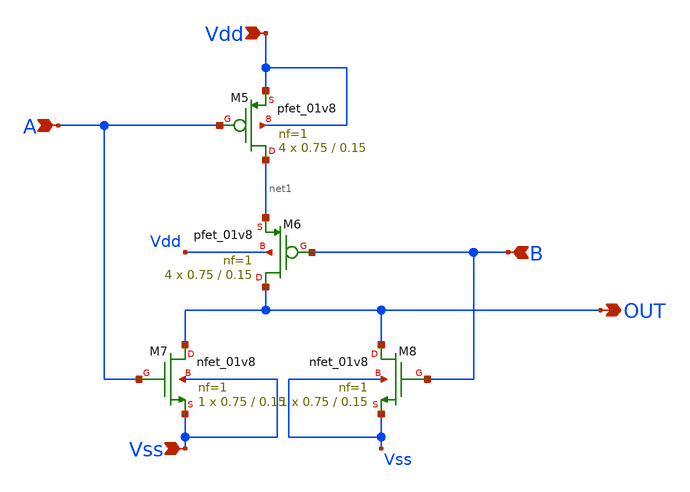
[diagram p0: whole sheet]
** sch_path: icdesign/sch/NOR/NOR.sch
**.subckt NOR Vdd Vss A B OUT
*.ipin Vdd
*.ipin Vss
*.ipin A
*.ipin B
*.opin OUT
XM5 net1 A Vdd Vdd sky130_fd_pr__pfet_01v8 L=0.15 W=0.75 nf=1 ad='int((nf+1)/2) * W/nf * 0.29' as='int((nf+2)/2) * W/nf * 0.29'
+ pd='2*int((nf+1)/2) * (W/nf + 0.29)' ps='2*int((nf+2)/2) * (W/nf + 0.29)' nrd='0.29 / W' nrs='0.29 / W'
+ sa=0 sb=0 sd=0 mult=4 m=4
XM6 OUT B net1 Vdd sky130_fd_pr__pfet_01v8 L=0.15 W=0.75 nf=1 ad='int((nf+1)/2) * W/nf * 0.29' as='int((nf+2)/2) * W/nf * 0.29'
+ pd='2*int((nf+1)/2) * (W/nf + 0.29)' ps='2*int((nf+2)/2) * (W/nf + 0.29)' nrd='0.29 / W' nrs='0.29 / W'
+ sa=0 sb=0 sd=0 mult=4 m=4
XM7 OUT A Vss Vss sky130_fd_pr__nfet_01v8 L=0.15 W=0.75 nf=1 ad='int((nf+1)/2) * W/nf * 0.29' as='int((nf+2)/2) * W/nf * 0.29'
+ pd='2*int((nf+1)/2) * (W/nf + 0.29)' ps='2*int((nf+2)/2) * (W/nf + 0.29)' nrd='0.29 / W' nrs='0.29 / W'
+ sa=0 sb=0 sd=0 mult=1 m=1
XM8 OUT B Vss Vss sky130_fd_pr__nfet_01v8 L=0.15 W=0.75 nf=1 ad='int((nf+1)/2) * W/nf * 0.29' as='int((nf+2)/2) * W/nf * 0.29'
+ pd='2*int((nf+1)/2) * (W/nf + 0.29)' ps='2*int((nf+2)/2) * (W/nf + 0.29)' nrd='0.29 / W' nrs='0.29 / W'
+ sa=0 sb=0 sd=0 mult=1 m=1
**.ends
.end
